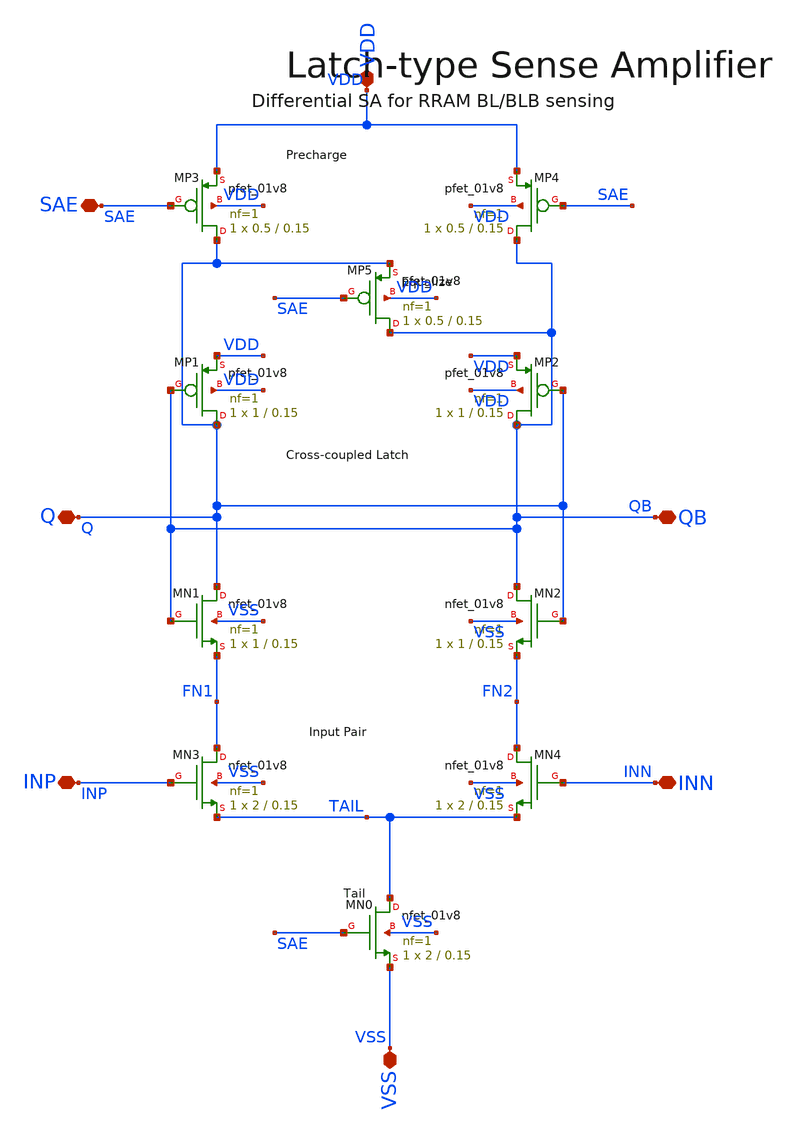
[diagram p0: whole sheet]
** sch_path: analog/xschem/xschem/sense_amp.sch
**.subckt sense_amp SAE INP INN Q QB VDD VSS
*.iopin SAE
*.iopin INP
*.iopin INN
*.iopin Q
*.iopin QB
*.iopin VDD
*.iopin VSS
XMP3 Q SAE VDD VDD sky130_fd_pr__pfet_01v8 L=0.15 W=0.5 nf=1 ad='int((nf+1)/2) * W/nf * 0.29' as='int((nf+2)/2) * W/nf * 0.29'
+ pd='2*int((nf+1)/2) * (W/nf + 0.29)' ps='2*int((nf+2)/2) * (W/nf + 0.29)' nrd='0.29 / W' nrs='0.29 / W'
+ sa=0 sb=0 sd=0 mult=1 m=1
XMP4 QB SAE VDD VDD sky130_fd_pr__pfet_01v8 L=0.15 W=0.5 nf=1 ad='int((nf+1)/2) * W/nf * 0.29' as='int((nf+2)/2) * W/nf * 0.29'
+ pd='2*int((nf+1)/2) * (W/nf + 0.29)' ps='2*int((nf+2)/2) * (W/nf + 0.29)' nrd='0.29 / W' nrs='0.29 / W'
+ sa=0 sb=0 sd=0 mult=1 m=1
XMP5 QB SAE Q VDD sky130_fd_pr__pfet_01v8 L=0.15 W=0.5 nf=1 ad='int((nf+1)/2) * W/nf * 0.29' as='int((nf+2)/2) * W/nf * 0.29'
+ pd='2*int((nf+1)/2) * (W/nf + 0.29)' ps='2*int((nf+2)/2) * (W/nf + 0.29)' nrd='0.29 / W' nrs='0.29 / W'
+ sa=0 sb=0 sd=0 mult=1 m=1
XMP1 Q QB VDD VDD sky130_fd_pr__pfet_01v8 L=0.15 W=1 nf=1 ad='int((nf+1)/2) * W/nf * 0.29' as='int((nf+2)/2) * W/nf * 0.29'
+ pd='2*int((nf+1)/2) * (W/nf + 0.29)' ps='2*int((nf+2)/2) * (W/nf + 0.29)' nrd='0.29 / W' nrs='0.29 / W'
+ sa=0 sb=0 sd=0 mult=1 m=1
XMP2 QB Q VDD VDD sky130_fd_pr__pfet_01v8 L=0.15 W=1 nf=1 ad='int((nf+1)/2) * W/nf * 0.29' as='int((nf+2)/2) * W/nf * 0.29'
+ pd='2*int((nf+1)/2) * (W/nf + 0.29)' ps='2*int((nf+2)/2) * (W/nf + 0.29)' nrd='0.29 / W' nrs='0.29 / W'
+ sa=0 sb=0 sd=0 mult=1 m=1
XMN1 Q QB FN1 VSS sky130_fd_pr__nfet_01v8 L=0.15 W=1 nf=1 ad='int((1 + 1)/2) * 1 / 1 * 0.29' as='int((1 + 2)/2) * 1 / 1 * 0.29'
+ pd='2*int((1 + 1)/2) * (1 / 1 + 0.29)' ps='2*int((1 + 2)/2) * (1 / 1 + 0.29)' nrd='0.29 / 1 ' nrs='0.29 / 1 '
+ sa=0 sb=0 sd=0 mult=1 m=1
XMN2 QB Q FN2 VSS sky130_fd_pr__nfet_01v8 L=0.15 W=1 nf=1 ad='int((1 + 1)/2) * 1 / 1 * 0.29' as='int((1 + 2)/2) * 1 / 1 * 0.29'
+ pd='2*int((1 + 1)/2) * (1 / 1 + 0.29)' ps='2*int((1 + 2)/2) * (1 / 1 + 0.29)' nrd='0.29 / 1 ' nrs='0.29 / 1 '
+ sa=0 sb=0 sd=0 mult=1 m=1
XMN3 FN1 INP TAIL VSS sky130_fd_pr__nfet_01v8 L=0.15 W=2 nf=1 ad='int((1 + 1)/2) * 2 / 1 * 0.29' as='int((1 + 2)/2) * 2 / 1 * 0.29'
+ pd='2*int((1 + 1)/2) * (2 / 1 + 0.29)' ps='2*int((1 + 2)/2) * (2 / 1 + 0.29)' nrd='0.29 / 2 ' nrs='0.29 / 2 '
+ sa=0 sb=0 sd=0 mult=1 m=1
XMN4 FN2 INN TAIL VSS sky130_fd_pr__nfet_01v8 L=0.15 W=2 nf=1 ad='int((1 + 1)/2) * 2 / 1 * 0.29' as='int((1 + 2)/2) * 2 / 1 * 0.29'
+ pd='2*int((1 + 1)/2) * (2 / 1 + 0.29)' ps='2*int((1 + 2)/2) * (2 / 1 + 0.29)' nrd='0.29 / 2 ' nrs='0.29 / 2 '
+ sa=0 sb=0 sd=0 mult=1 m=1
XMN0 TAIL SAE VSS VSS sky130_fd_pr__nfet_01v8 L=0.15 W=2 nf=1 ad='int((1 + 1)/2) * 2 / 1 * 0.29' as='int((1 + 2)/2) * 2 / 1 * 0.29'
+ pd='2*int((1 + 1)/2) * (2 / 1 + 0.29)' ps='2*int((1 + 2)/2) * (2 / 1 + 0.29)' nrd='0.29 / 2 ' nrs='0.29 / 2 '
+ sa=0 sb=0 sd=0 mult=1 m=1
**.ends
.end
